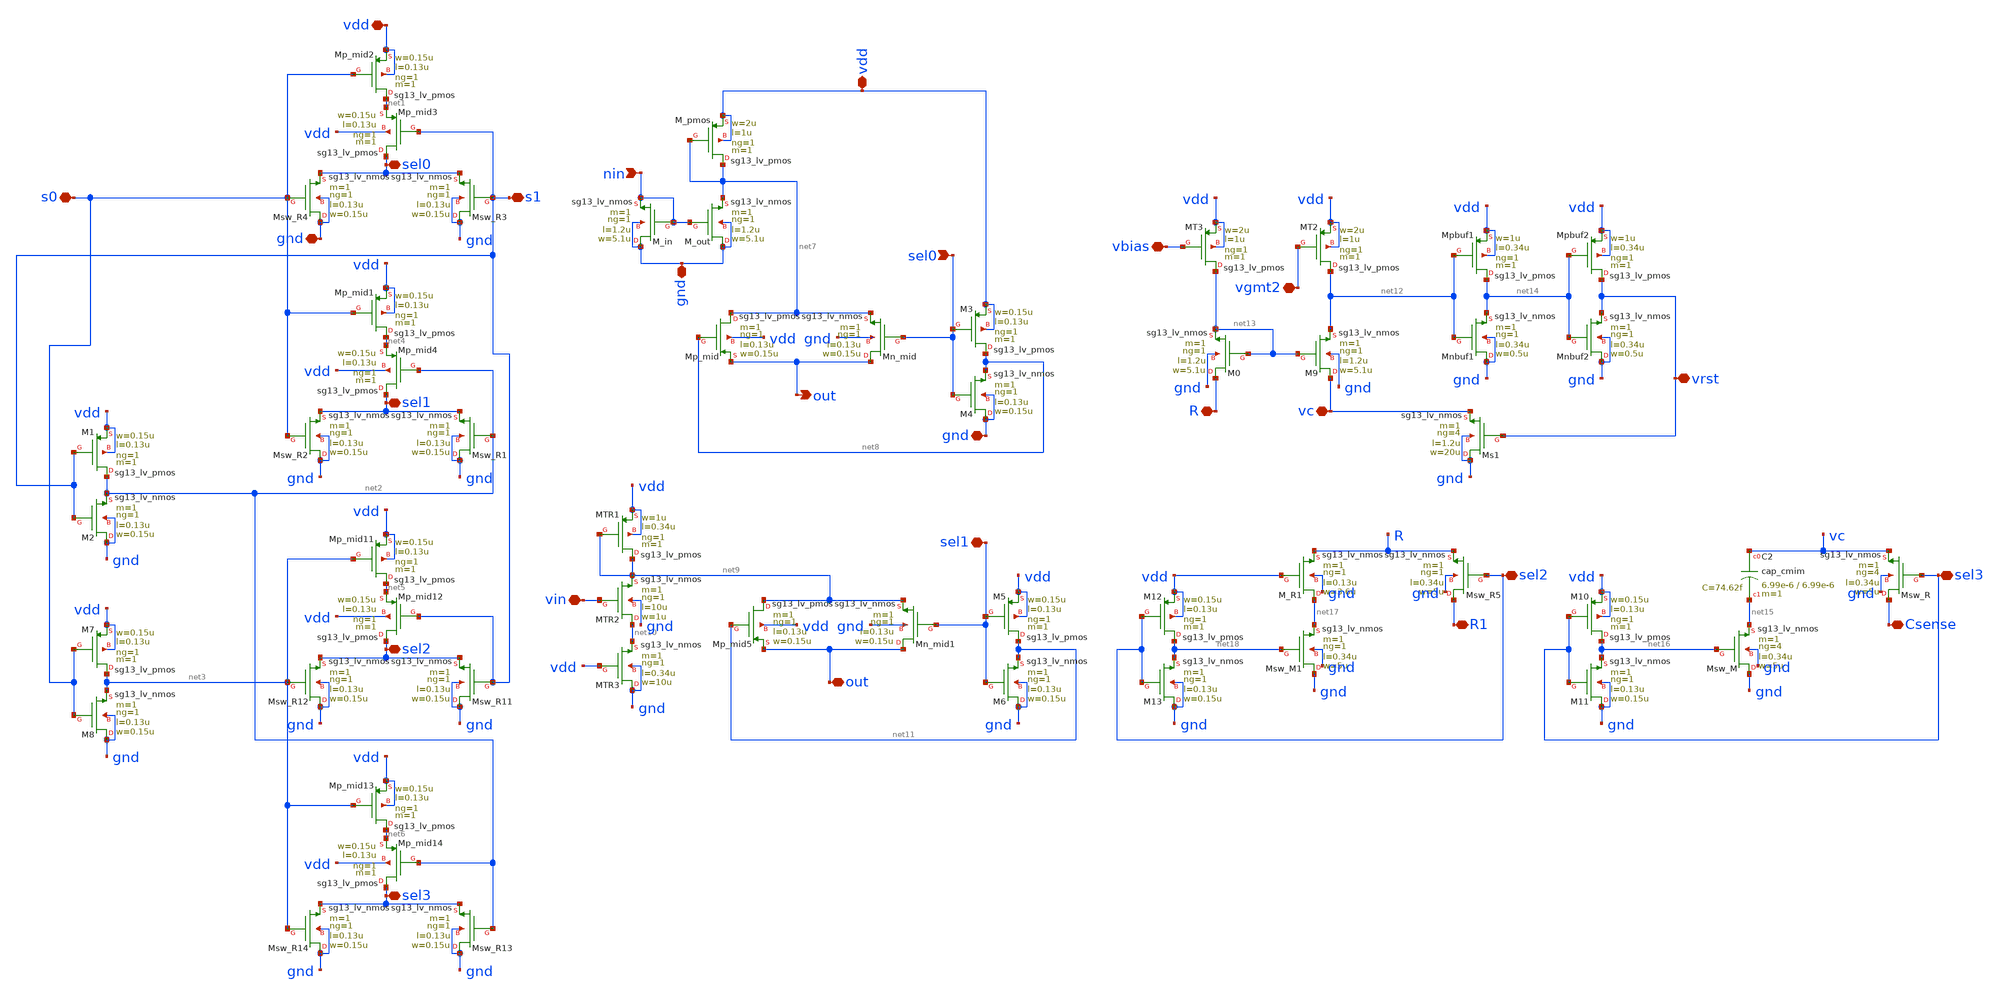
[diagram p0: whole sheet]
** sch_path: Enfoque_B/xschem/referencia/ASIC_TOP_plano.sch
**.subckt ASIC_TOP_plano s1 s0 vdd gnd sel0 sel1 sel2 sel3 out vin sel1 vbias vrst vc vgmt2 R sel3
*+ Csense sel2 R1 sel0 nin gnd out vdd gnd
*.iopin s1
*.iopin s0
*.iopin vdd
*.iopin gnd
*.iopin sel0
*.iopin sel1
*.iopin sel2
*.iopin sel3
*.iopin out
*.iopin vin
*.iopin sel1
*.iopin vbias
*.iopin vrst
*.iopin vc
*.iopin vgmt2
*.iopin R
*.iopin sel3
*.iopin Csense
*.iopin sel2
*.iopin R1
*.ipin sel0
*.ipin nin
*.iopin gnd
*.opin out
*.iopin vdd
*.iopin gnd
XMp_mid2 net1 s0 vdd vdd sg13_lv_pmos w=0.15u l=0.13u ng=1 m=1 mm_ok=1
XMp_mid3 sel0 s1 net1 vdd sg13_lv_pmos w=0.15u l=0.13u ng=1 m=1 mm_ok=1
XMsw_R3 gnd s1 sel0 gnd sg13_lv_nmos w=0.15u l=0.13u ng=1 m=1 mm_ok=1
XMsw_R4 gnd s0 sel0 gnd sg13_lv_nmos w=0.15u l=0.13u ng=1 m=1 mm_ok=1
XM1 net2 s1 vdd vdd sg13_lv_pmos w=0.15u l=0.13u ng=1 m=1 mm_ok=1
XM2 gnd s1 net2 gnd sg13_lv_nmos w=0.15u l=0.13u ng=1 m=1 mm_ok=1
XM7 net3 s0 vdd vdd sg13_lv_pmos w=0.15u l=0.13u ng=1 m=1 mm_ok=1
XM8 gnd s0 net3 gnd sg13_lv_nmos w=0.15u l=0.13u ng=1 m=1 mm_ok=1
XMp_mid1 net4 s0 vdd vdd sg13_lv_pmos w=0.15u l=0.13u ng=1 m=1 mm_ok=1
XMp_mid4 sel1 net2 net4 vdd sg13_lv_pmos w=0.15u l=0.13u ng=1 m=1 mm_ok=1
XMsw_R1 gnd net2 sel1 gnd sg13_lv_nmos w=0.15u l=0.13u ng=1 m=1 mm_ok=1
XMsw_R2 gnd s0 sel1 gnd sg13_lv_nmos w=0.15u l=0.13u ng=1 m=1 mm_ok=1
XMp_mid11 net5 net3 vdd vdd sg13_lv_pmos w=0.15u l=0.13u ng=1 m=1 mm_ok=1
XMp_mid12 sel2 s1 net5 vdd sg13_lv_pmos w=0.15u l=0.13u ng=1 m=1 mm_ok=1
XMsw_R11 gnd s1 sel2 gnd sg13_lv_nmos w=0.15u l=0.13u ng=1 m=1 mm_ok=1
XMsw_R12 gnd net3 sel2 gnd sg13_lv_nmos w=0.15u l=0.13u ng=1 m=1 mm_ok=1
XMp_mid13 net6 net3 vdd vdd sg13_lv_pmos w=0.15u l=0.13u ng=1 m=1 mm_ok=1
XMp_mid14 sel3 net2 net6 vdd sg13_lv_pmos w=0.15u l=0.13u ng=1 m=1 mm_ok=1
XMsw_R13 gnd net2 sel3 gnd sg13_lv_nmos w=0.15u l=0.13u ng=1 m=1 mm_ok=1
XMsw_R14 gnd net3 sel3 gnd sg13_lv_nmos w=0.15u l=0.13u ng=1 m=1 mm_ok=1
XM_out gnd nin net7 gnd sg13_lv_nmos w=5.1u l=1.2u ng=1 m=1 mm_ok=1
XM_pmos net7 net7 vdd vdd sg13_lv_pmos w=2u l=1u ng=1 m=1 mm_ok=1
XM_in gnd nin nin gnd sg13_lv_nmos w=5.1u l=1.2u ng=1 m=1 mm_ok=1
XMn_mid out sel0 net7 gnd sg13_lv_nmos w=0.15u l=0.13u ng=1 m=1 mm_ok=1
XMp_mid net7 net8 out vdd sg13_lv_pmos w=0.15u l=0.13u ng=1 m=1 mm_ok=1
XM3 net8 sel0 vdd vdd sg13_lv_pmos w=0.15u l=0.13u ng=1 m=1 mm_ok=1
XM4 gnd sel0 net8 gnd sg13_lv_nmos w=0.15u l=0.13u ng=1 m=1 mm_ok=1
XMTR1 net9 net9 vdd vdd sg13_lv_pmos w=1u l=0.34u ng=1 m=1 mm_ok=1
XMTR2 net10 vin net9 gnd sg13_lv_nmos w=1u l=10u ng=1 m=1 mm_ok=1
XMTR3 gnd vdd net10 gnd sg13_lv_nmos w=10u l=0.34u ng=1 m=1 mm_ok=1
XMn_mid1 out sel1 net9 gnd sg13_lv_nmos w=0.15u l=0.13u ng=1 m=1 mm_ok=1
XMp_mid5 net9 net11 out vdd sg13_lv_pmos w=0.15u l=0.13u ng=1 m=1 mm_ok=1
XM5 net11 sel1 vdd vdd sg13_lv_pmos w=0.15u l=0.13u ng=1 m=1 mm_ok=1
XM6 gnd sel1 net11 gnd sg13_lv_nmos w=0.15u l=0.13u ng=1 m=1 mm_ok=1
XMT3 net13 vbias vdd vdd sg13_lv_pmos w=2u l=1u ng=1 m=1 mm_ok=1
XMT2 net12 vgmt2 vdd vdd sg13_lv_pmos w=2u l=1u ng=1 m=1 mm_ok=1
XM9 vc net13 net12 gnd sg13_lv_nmos w=5.1u l=1.2u ng=1 m=1 mm_ok=1
XM0 R net13 net13 gnd sg13_lv_nmos w=5.1u l=1.2u ng=1 m=1 mm_ok=1
XMpbuf2 vrst net14 vdd vdd sg13_lv_pmos w=1u l=0.34u ng=1 m=1 mm_ok=1
XMnbuf1 gnd net12 net14 gnd sg13_lv_nmos w=0.5u l=0.34u ng=1 m=1 mm_ok=1
XMnbuf2 gnd net14 vrst gnd sg13_lv_nmos w=0.5u l=0.34u ng=1 m=1 mm_ok=1
XMs1 gnd vrst vc gnd sg13_lv_nmos w=20u l=1.2u ng=4 m=1 mm_ok=1
XMpbuf1 net14 net12 vdd vdd sg13_lv_pmos w=1u l=0.34u ng=1 m=1 mm_ok=1
XMsw_R Csense sel3 vc gnd sg13_lv_nmos w=5u l=0.34u ng=4 m=1 mm_ok=1
XMsw_M gnd net16 net15 gnd sg13_lv_nmos w=5u l=0.34u ng=4 m=1 mm_ok=1
XM10 net16 sel3 vdd vdd sg13_lv_pmos w=0.15u l=0.13u ng=1 m=1 mm_ok=1
XM11 gnd sel3 net16 gnd sg13_lv_nmos w=0.15u l=0.13u ng=1 m=1 mm_ok=1
XC2 vc net15 cap_cmim w=6.99e-6 l=6.99e-6 m=1 mm_ok=1
XMsw_R5 R1 sel2 R gnd sg13_lv_nmos w=5u l=0.34u ng=1 m=1 mm_ok=1
XM_R1 net17 vdd R gnd sg13_lv_nmos w=3.6u l=0.13u ng=1 m=1 mm_ok=1
XMsw_M1 gnd net18 net17 gnd sg13_lv_nmos w=5u l=0.34u ng=1 m=1 mm_ok=1
XM12 net18 sel2 vdd vdd sg13_lv_pmos w=0.15u l=0.13u ng=1 m=1 mm_ok=1
XM13 gnd sel2 net18 gnd sg13_lv_nmos w=0.15u l=0.13u ng=1 m=1 mm_ok=1
**.ends
.end
